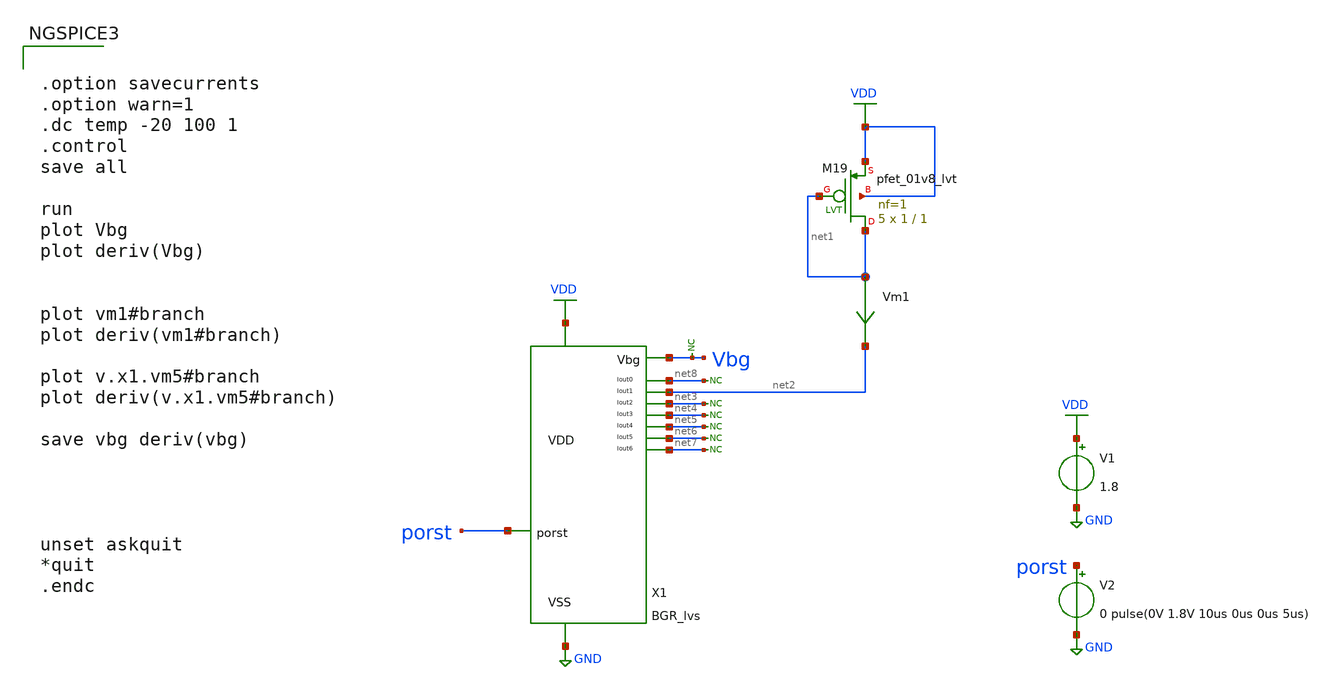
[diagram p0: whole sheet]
** sch_path: design/bgr_new/tb_BGR_pvt_lvs.sch
**.subckt tb_BGR_pvt_lvs
V1 VDD GND 1.8
V2 porst GND 0 pulse(0V 1.8V 10us 0us 0us 5us)
XM19 net1 net1 VDD VDD sky130_fd_pr__pfet_01v8_lvt L=1 W=1 nf=1 ad='int((nf+1)/2) * W/nf * 0.29' as='int((nf+2)/2) * W/nf * 0.29'
+ pd='2*int((nf+1)/2) * (W/nf + 0.29)' ps='2*int((nf+2)/2) * (W/nf + 0.29)' nrd='0.29 / W' nrs='0.29 / W'
+ sa=0 sb=0 sd=0 mult=5 m=5
Vm1 net1 net2 0
.save i(vm1)
* noconn Vbg
* noconn #net3
* noconn #net4
* noconn #net5
* noconn #net6
* noconn #net7
* noconn #net8
X1 porst VDD GND Vbg net8 net2 net3 net4 net5 net6 net7 BGR_lvs
**** begin user architecture code

** opencircuitdesign pdks install
.lib $::SKYWATER_MODELS/sky130.lib.spice tt




.option savecurrents
.option warn=1
.dc temp -20 100 1
.control
save all

run
plot Vbg
plot deriv(Vbg)


plot vm1#branch
plot deriv(vm1#branch)

plot v.x1.vm5#branch
plot deriv(v.x1.vm5#branch)

save vbg deriv(vbg)




unset askquit
*quit
.endc


**** end user architecture code
**.ends
.GLOBAL VDD
.GLOBAL GND
.end
